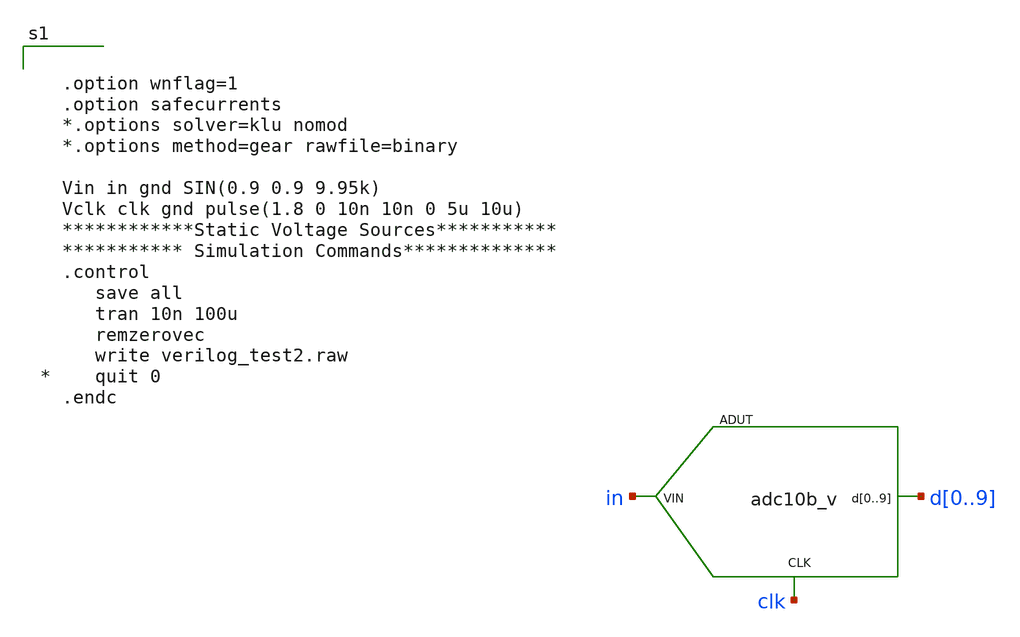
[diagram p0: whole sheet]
** sch_path: xschem/verilog_test.sch
**.subckt verilog_test
ADUT [ in clk ] [ d0 d1 d2 d3 d4 d5 d6 d7 d8 d9 ] dut
**** begin user architecture code


  .option wnflag=1
  .option safecurrents
  *.options solver=klu nomod
  *.options method=gear rawfile=binary

  Vin in gnd SIN(0.9 0.9 9.95k)
  Vclk clk gnd pulse(1.8 0 10n 10n 0 5u 10u)
  ************Static Voltage Sources***********
  *********** Simulation Commands**************
  .control
     save all
     tran 10n 100u
     remzerovec
     write verilog_test2.raw
*    quit 0
  .endc


**** end user architecture code
**.ends
**** begin user architecture code
.model dut d_cosim simulation="ivlng" sim_args=["adc"]
**** end user architecture code
.end
